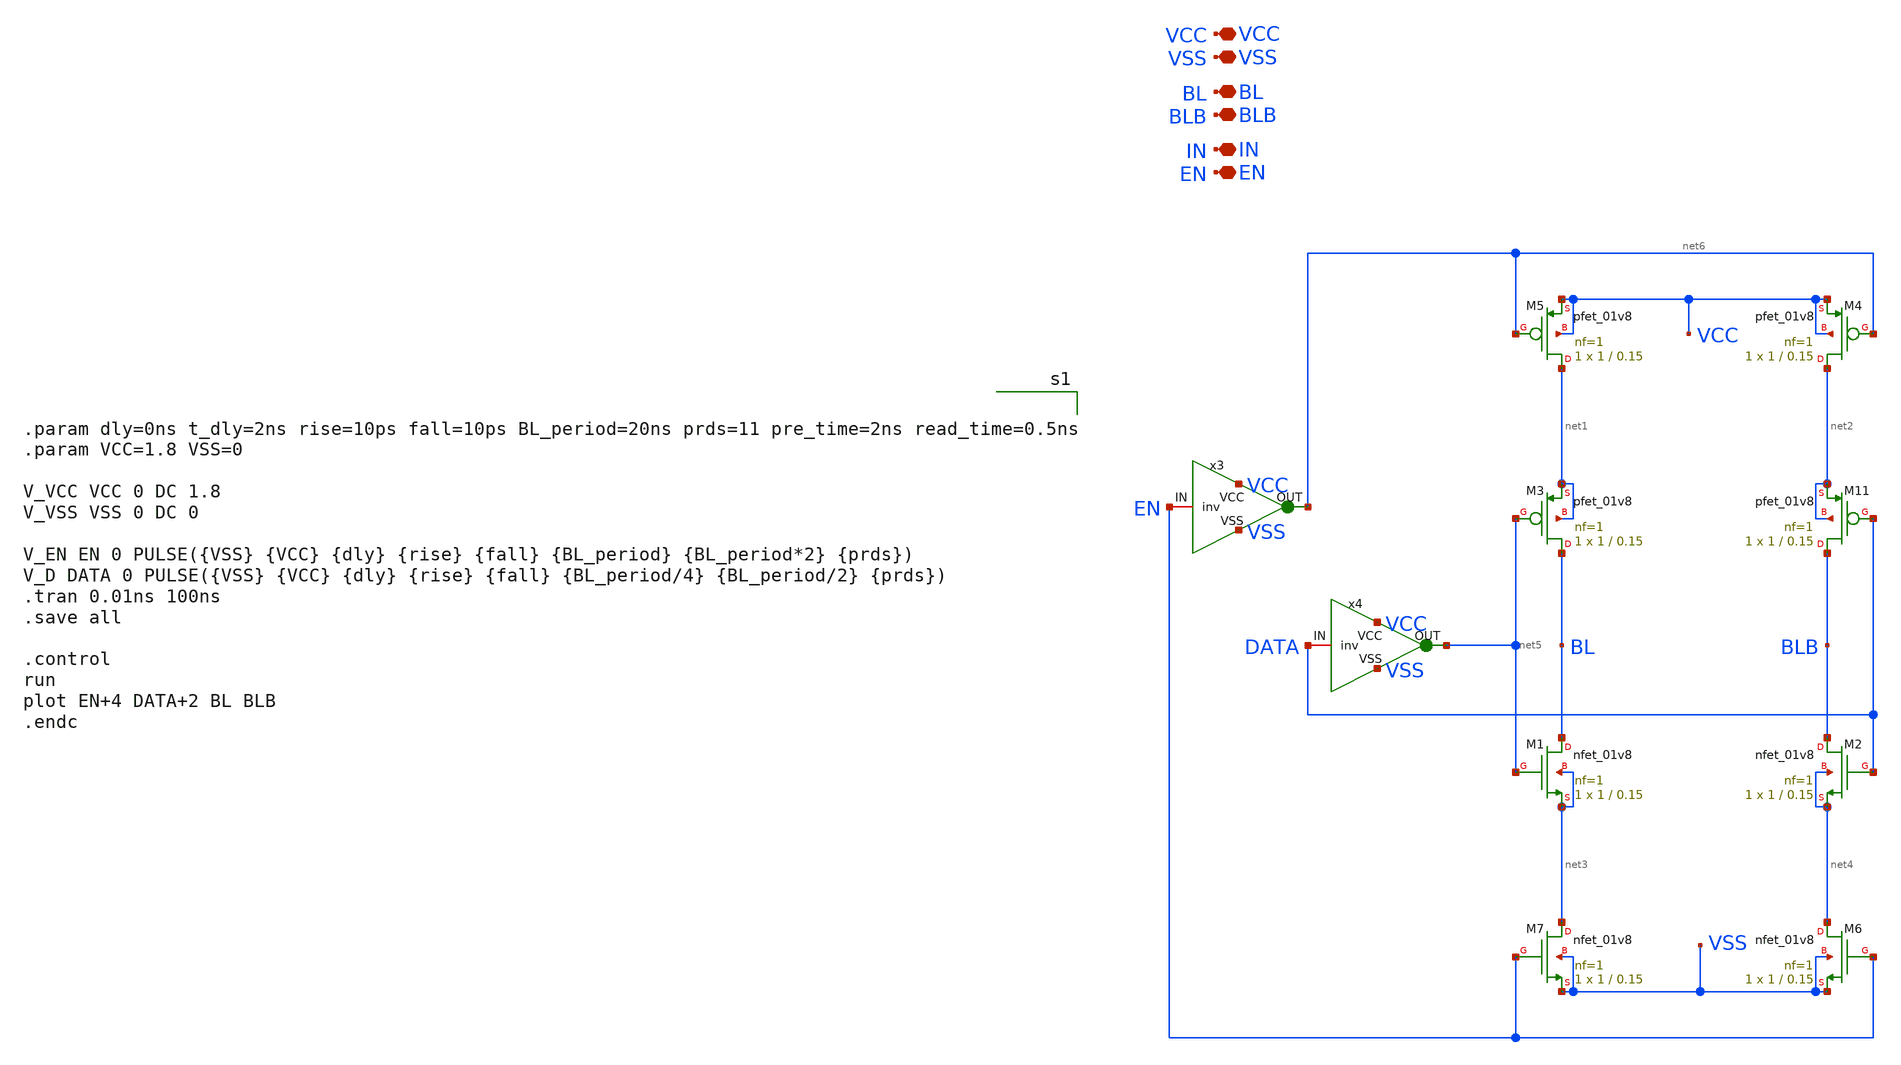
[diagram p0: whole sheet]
** sch_path: peripherals/write_driver2.sch
**.subckt write_driver2 VCC VSS BL BLB IN EN
*.iopin VCC
*.iopin VSS
*.iopin BL
*.iopin BLB
*.iopin IN
*.iopin EN
XM2 BLB DATA net4 net4 sky130_fd_pr__nfet_01v8 L=0.15 W=1 nf=1 ad='int((1 + 1)/2) * 1 / 1 * 0.29' as='int((1 + 2)/2) * 1 / 1 * 0.29'
+ pd='2*int((1 + 1)/2) * (1 / 1 + 0.29)' ps='2*int((1 + 2)/2) * (1 / 1 + 0.29)' nrd='0.29 / 1 ' nrs='0.29 / 1 '
+ sa=0 sb=0 sd=0 mult=1 m=1
XM11 BLB DATA net2 net2 sky130_fd_pr__pfet_01v8 L=0.15 W=1 nf=1 ad='int((nf+1)/2) * W/nf * 0.29' as='int((nf+2)/2) * W/nf * 0.29'
+ pd='2*int((nf+1)/2) * (W/nf + 0.29)' ps='2*int((nf+2)/2) * (W/nf + 0.29)' nrd='0.29 / W' nrs='0.29 / W'
+ sa=0 sb=0 sd=0 mult=1 m=1
XM1 BL net5 net3 net3 sky130_fd_pr__nfet_01v8 L=0.15 W=1 nf=1 ad='int((1 + 1)/2) * 1 / 1 * 0.29' as='int((1 + 2)/2) * 1 / 1 * 0.29'
+ pd='2*int((1 + 1)/2) * (1 / 1 + 0.29)' ps='2*int((1 + 2)/2) * (1 / 1 + 0.29)' nrd='0.29 / 1 ' nrs='0.29 / 1 '
+ sa=0 sb=0 sd=0 mult=1 m=1
XM3 BL net5 net1 net1 sky130_fd_pr__pfet_01v8 L=0.15 W=1 nf=1 ad='int((nf+1)/2) * W/nf * 0.29' as='int((nf+2)/2) * W/nf * 0.29'
+ pd='2*int((nf+1)/2) * (W/nf + 0.29)' ps='2*int((nf+2)/2) * (W/nf + 0.29)' nrd='0.29 / W' nrs='0.29 / W'
+ sa=0 sb=0 sd=0 mult=1 m=1
XM4 net2 net6 VCC VCC sky130_fd_pr__pfet_01v8 L=0.15 W=1 nf=1 ad='int((nf+1)/2) * W/nf * 0.29' as='int((nf+2)/2) * W/nf * 0.29'
+ pd='2*int((nf+1)/2) * (W/nf + 0.29)' ps='2*int((nf+2)/2) * (W/nf + 0.29)' nrd='0.29 / W' nrs='0.29 / W'
+ sa=0 sb=0 sd=0 mult=1 m=1
XM5 net1 net6 VCC VCC sky130_fd_pr__pfet_01v8 L=0.15 W=1 nf=1 ad='int((nf+1)/2) * W/nf * 0.29' as='int((nf+2)/2) * W/nf * 0.29'
+ pd='2*int((nf+1)/2) * (W/nf + 0.29)' ps='2*int((nf+2)/2) * (W/nf + 0.29)' nrd='0.29 / W' nrs='0.29 / W'
+ sa=0 sb=0 sd=0 mult=1 m=1
XM6 net4 EN VSS VSS sky130_fd_pr__nfet_01v8 L=0.15 W=1 nf=1 ad='int((1 + 1)/2) * 1 / 1 * 0.29' as='int((1 + 2)/2) * 1 / 1 * 0.29'
+ pd='2*int((1 + 1)/2) * (1 / 1 + 0.29)' ps='2*int((1 + 2)/2) * (1 / 1 + 0.29)' nrd='0.29 / 1 ' nrs='0.29 / 1 '
+ sa=0 sb=0 sd=0 mult=1 m=1
XM7 net3 EN VSS VSS sky130_fd_pr__nfet_01v8 L=0.15 W=1 nf=1 ad='int((1 + 1)/2) * 1 / 1 * 0.29' as='int((1 + 2)/2) * 1 / 1 * 0.29'
+ pd='2*int((1 + 1)/2) * (1 / 1 + 0.29)' ps='2*int((1 + 2)/2) * (1 / 1 + 0.29)' nrd='0.29 / 1 ' nrs='0.29 / 1 '
+ sa=0 sb=0 sd=0 mult=1 m=1
x3 VCC EN net6 VSS inv
x4 VCC DATA net5 VSS inv
**** begin user architecture code


.param dly=0ns t_dly=2ns rise=10ps fall=10ps BL_period=20ns prds=11 pre_time=2ns read_time=0.5ns
.param VCC=1.8 VSS=0

V_VCC VCC 0 DC 1.8
V_VSS VSS 0 DC 0

V_EN EN 0 PULSE({VSS} {VCC} {dly} {rise} {fall} {BL_period} {BL_period*2} {prds})
V_D DATA 0 PULSE({VSS} {VCC} {dly} {rise} {fall} {BL_period/4} {BL_period/2} {prds})
.tran 0.01ns 100ns
.save all

.control
run
plot EN+4 DATA+2 BL BLB
.endc



** opencircuitdesign pdks install
.lib $::SKYWATER_MODELS/sky130.lib.spice tt

**** end user architecture code
**.ends

* expanding   symbol:  inv.sym # of pins=4
** sym_path: peripherals/inv.sym
** sch_path: peripherals/inv.sch
.subckt inv VCC IN OUT VSS
*.iopin VCC
*.iopin IN
*.iopin OUT
*.iopin VSS
XM1 OUT IN VSS VSS sky130_fd_pr__nfet_01v8 L=0.15 W=0.5 nf=1 ad='int((nf+1)/2) * W/nf * 0.29' as='int((nf+2)/2) * W/nf * 0.29'
+ pd='2*int((nf+1)/2) * (W/nf + 0.29)' ps='2*int((nf+2)/2) * (W/nf + 0.29)' nrd='0.29 / W' nrs='0.29 / W'
+ sa=0 sb=0 sd=0 mult=1 m=1
XM2 OUT IN VCC VCC sky130_fd_pr__pfet_01v8 L=0.15 W=1.05 nf=1 ad='int((nf+1)/2) * W/nf * 0.29' as='int((nf+2)/2) * W/nf * 0.29'
+ pd='2*int((nf+1)/2) * (W/nf + 0.29)' ps='2*int((nf+2)/2) * (W/nf + 0.29)' nrd='0.29 / W' nrs='0.29 / W'
+ sa=0 sb=0 sd=0 mult=1 m=1
.ends

.end
